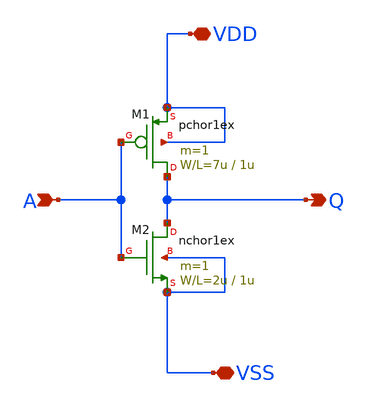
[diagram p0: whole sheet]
** sch_path: member_project/passiven/test7_2.sch
**.subckt test7_2 A Q VDD VSS
*.ipin A
*.opin Q
*.iopin VDD
*.iopin VSS
M1 Q A VDD VDD pchor1ex L=1u W=7u m=1
M2 Q A VSS VSS nchor1ex L=1u W=2u m=1
**.ends
.end
